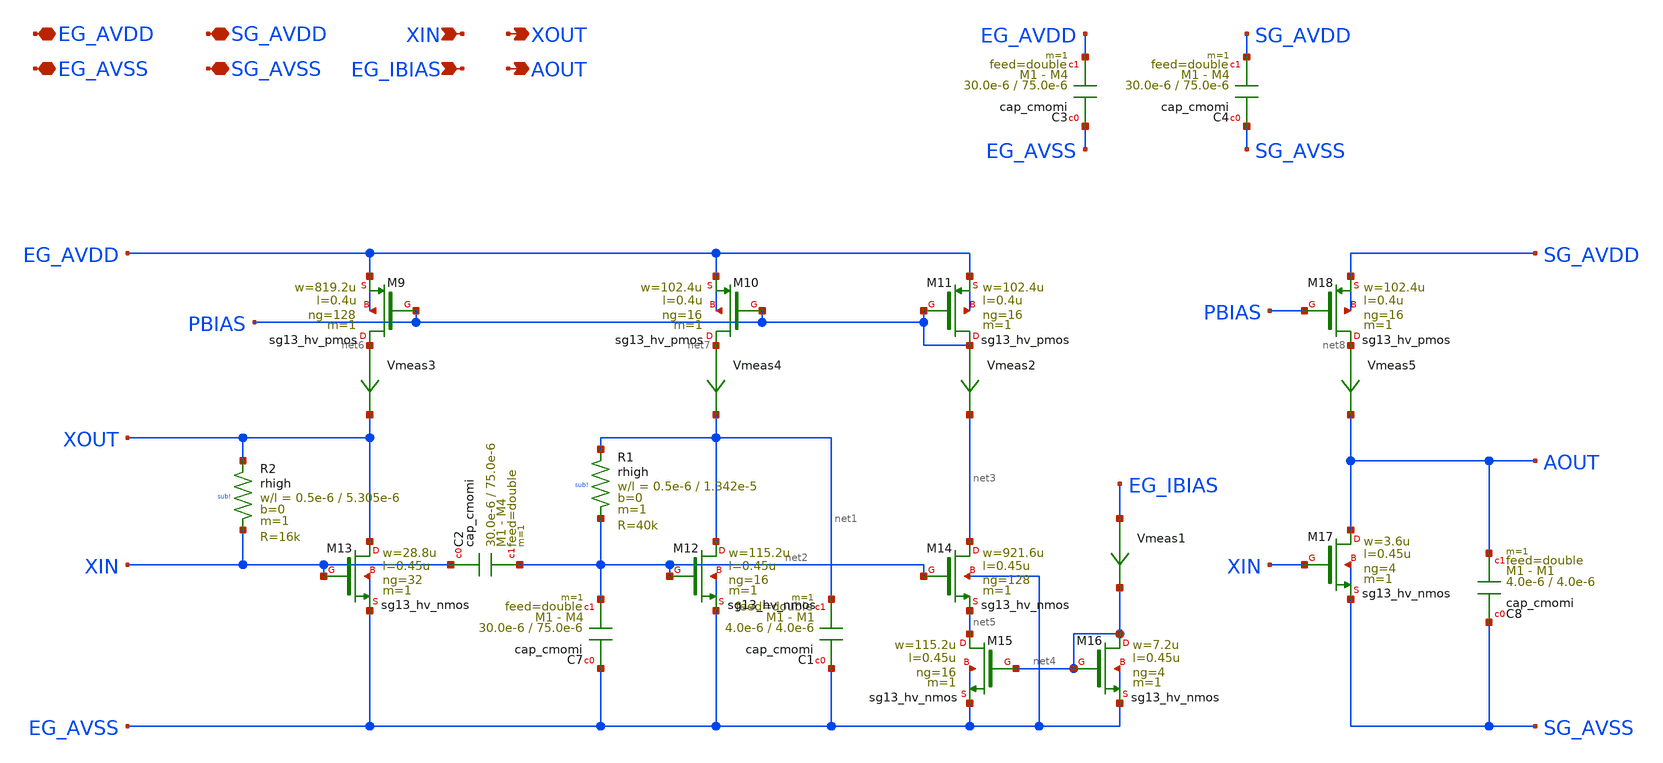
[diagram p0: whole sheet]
** sch_path: xschem/vittoz_pierce_osc.sch
**.subckt vittoz_pierce_osc EG_AVDD EG_AVSS SG_AVDD SG_AVSS XIN EG_IBIAS XOUT AOUT
*.iopin EG_AVDD
*.iopin EG_AVSS
*.iopin SG_AVDD
*.iopin SG_AVSS
*.ipin XIN
*.ipin EG_IBIAS
*.opin XOUT
*.opin AOUT
Vmeas3 net6 XOUT 0
.save i(vmeas3)
Vmeas4 net7 net1 0
.save i(vmeas4)
Vmeas2 PBIAS net3 0
.save i(vmeas2)
Vmeas5 net8 AOUT 0
.save i(vmeas5)
Vmeas1 EG_IBIAS net4 0
.save i(vmeas1)
XC3 EG_AVSS EG_AVDD cap_cmomi w=30.0e-6 l=75.0e-6 mmin=1 mmax=4 feed=double subblock=0 m=1 mm_ok=1
XC4 SG_AVSS SG_AVDD cap_cmomi w=30.0e-6 l=75.0e-6 mmin=1 mmax=4 feed=double subblock=0 m=1 mm_ok=1
XR1 net1 net2 sub! rhigh w=0.5e-6 l=1.342e-5 m=1 b=0 mm_ok=1
XR2 XOUT XIN sub! rhigh w=0.5e-6 l=5.305e-6 m=1 b=0 mm_ok=1
XC2 XIN net2 cap_cmomi w=30.0e-6 l=75.0e-6 mmin=1 mmax=4 feed=double subblock=0 m=1 mm_ok=1
XC7 EG_AVSS net2 cap_cmomi w=30.0e-6 l=75.0e-6 mmin=1 mmax=4 feed=double subblock=0 m=1 mm_ok=1
XC1 EG_AVSS net1 cap_cmomi w=4.0e-6 l=4.0e-6 mmin=1 mmax=1 feed=double subblock=0 m=1 mm_ok=1
XC8 SG_AVSS AOUT cap_cmomi w=4.0e-6 l=4.0e-6 mmin=1 mmax=1 feed=double subblock=0 m=1 mm_ok=1
XM11 PBIAS PBIAS EG_AVDD EG_AVDD sg13_hv_pmos w=102.4u l=0.4u ng=16 m=1 mm_ok=1
XM10 net7 PBIAS EG_AVDD EG_AVDD sg13_hv_pmos w=102.4u l=0.4u ng=16 m=1 mm_ok=1
XM9 net6 PBIAS EG_AVDD EG_AVDD sg13_hv_pmos w=819.2u l=0.4u ng=128 m=1 mm_ok=1
XM14 net3 net2 net5 EG_AVSS sg13_hv_nmos w=921.6u l=0.45u ng=128 m=1 mm_ok=1
XM12 net1 net2 EG_AVSS EG_AVSS sg13_hv_nmos w=115.2u l=0.45u ng=16 m=1 mm_ok=1
XM13 XOUT XIN EG_AVSS EG_AVSS sg13_hv_nmos w=28.8u l=0.45u ng=32 m=1 mm_ok=1
XM15 net5 net4 EG_AVSS EG_AVSS sg13_hv_nmos w=115.2u l=0.45u ng=16 m=1 mm_ok=1
XM16 net4 net4 EG_AVSS EG_AVSS sg13_hv_nmos w=7.2u l=0.45u ng=4 m=1 mm_ok=1
XM18 net8 PBIAS SG_AVDD SG_AVDD sg13_hv_pmos w=102.4u l=0.4u ng=16 m=1 mm_ok=1
XM17 AOUT XIN SG_AVSS SG_AVSS sg13_hv_nmos w=3.6u l=0.45u ng=4 m=1 mm_ok=1
**.ends
.end
